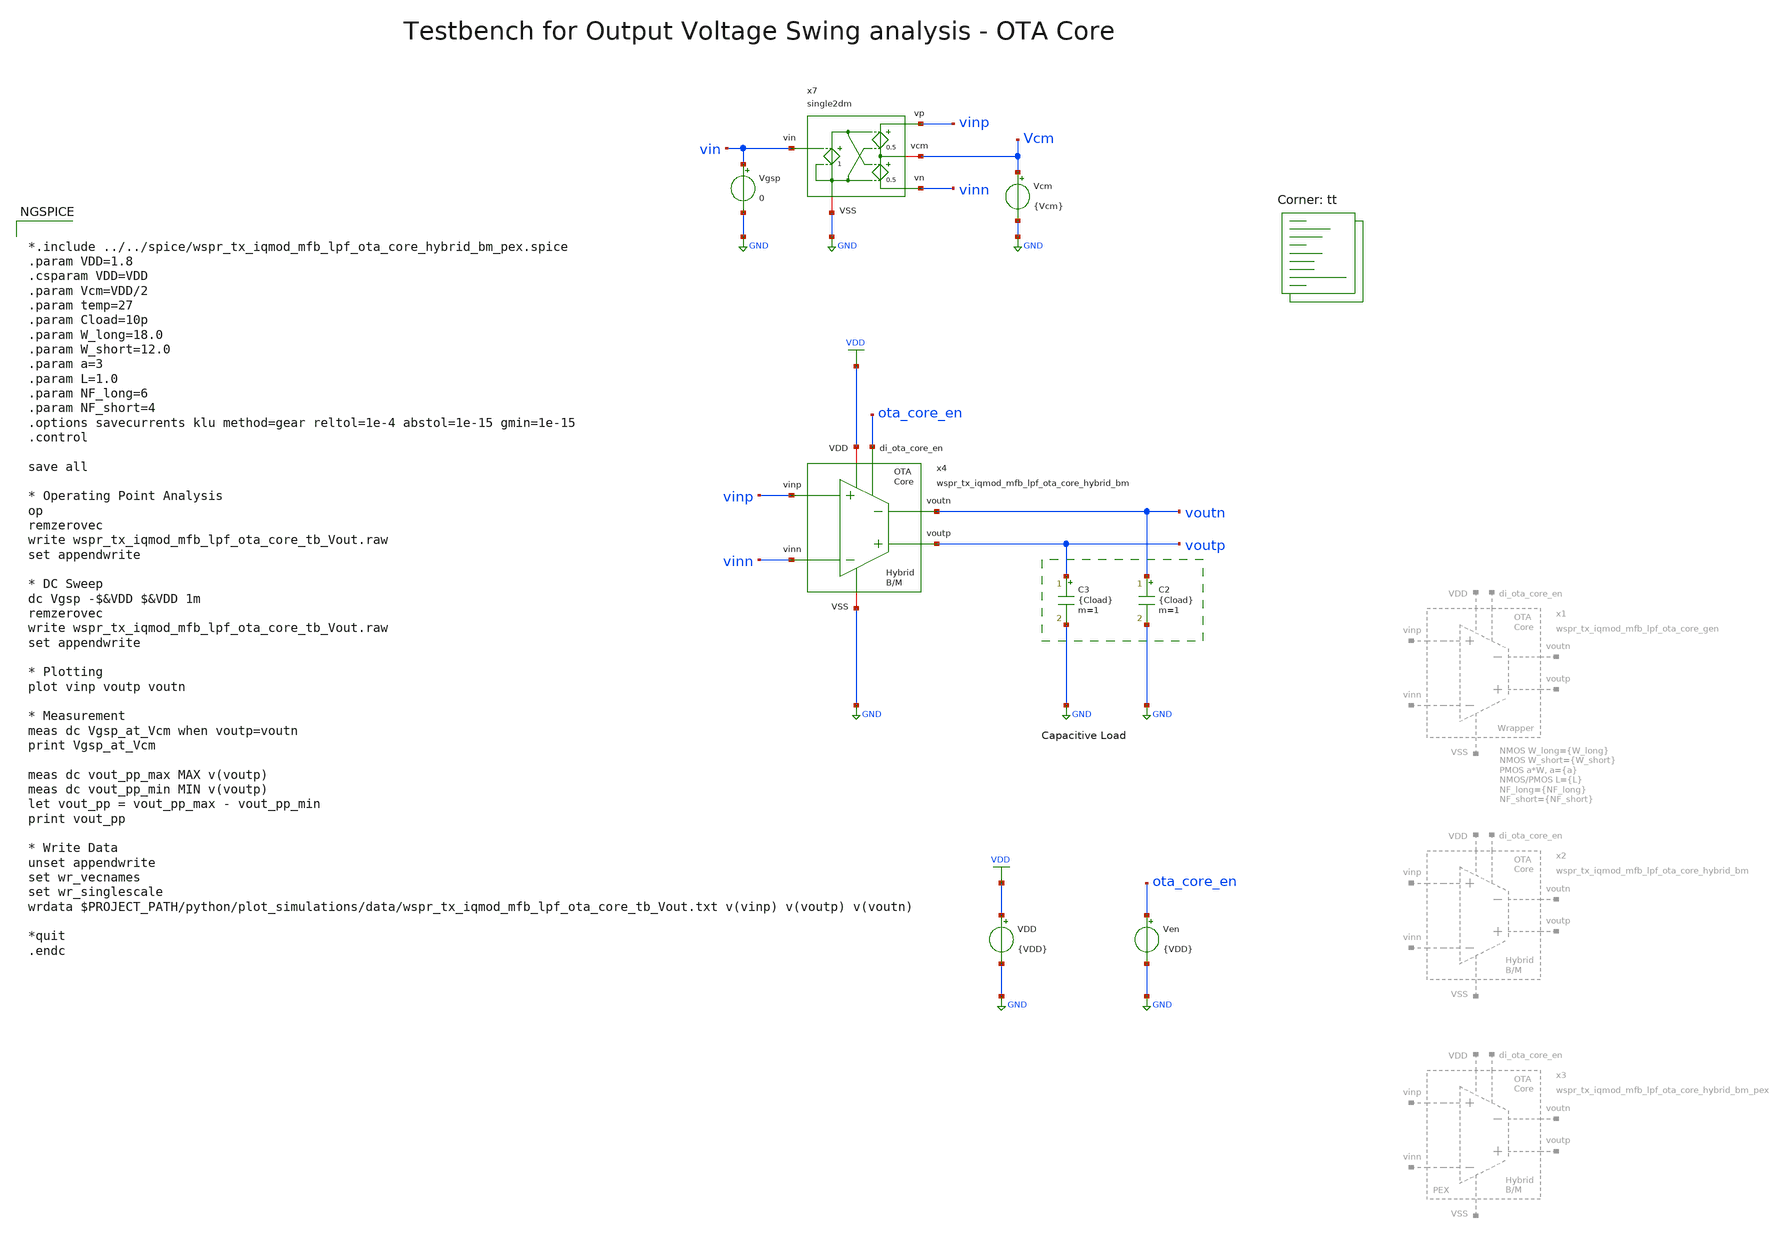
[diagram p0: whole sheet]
** sch_path: sky130/macros/iqmod/testbenches/wspr_tx_iqmod_mfb_lpf_ota_core_tb_Vout.sch
**.subckt wspr_tx_iqmod_mfb_lpf_ota_core_tb_Vout
VDD VDD GND {VDD}
Ven ota_core_en GND {VDD}
Vgsp vin GND 0
C2 voutn GND {Cload} m=1
C3 voutp GND {Cload} m=1
Vcm Vcm GND {Vcm}
x4 ota_core_en voutp voutn vinn vinp VDD GND wspr_tx_iqmod_mfb_lpf_ota_core_hybrid_bm
x7 vinp vin Vcm GND vinn single2dm
**** begin user architecture code


*.include ../../spice/wspr_tx_iqmod_mfb_lpf_ota_core_hybrid_bm_pex.spice
.param VDD=1.8
.csparam VDD=VDD
.param Vcm=VDD/2
.param temp=27
.param Cload=10p
.param W_long=18.0
.param W_short=12.0
.param a=3
.param L=1.0
.param NF_long=6
.param NF_short=4
.options savecurrents klu method=gear reltol=1e-4 abstol=1e-15 gmin=1e-15
.control

save all

* Operating Point Analysis
op
remzerovec
write wspr_tx_iqmod_mfb_lpf_ota_core_tb_Vout.raw
set appendwrite

* DC Sweep
dc Vgsp -$&VDD $&VDD 1m
remzerovec
write wspr_tx_iqmod_mfb_lpf_ota_core_tb_Vout.raw
set appendwrite

* Plotting
plot vinp voutp voutn

* Measurement
meas dc Vgsp_at_Vcm when voutp=voutn
print Vgsp_at_Vcm

meas dc vout_pp_max MAX v(voutp)
meas dc vout_pp_min MIN v(voutp)
let vout_pp = vout_pp_max - vout_pp_min
print vout_pp

* Write Data
unset appendwrite
set wr_vecnames
set wr_singlescale
wrdata $PROJECT_PATH/python/plot_simulations/data/wspr_tx_iqmod_mfb_lpf_ota_core_tb_Vout.txt v(vinp)
+ v(voutp) v(voutn)

*quit
.endc


.lib $::SKYWATER_MODELS/sky130.lib.spice tt
**** end user architecture code
**.ends
.GLOBAL GND
.GLOBAL VDD
.end
